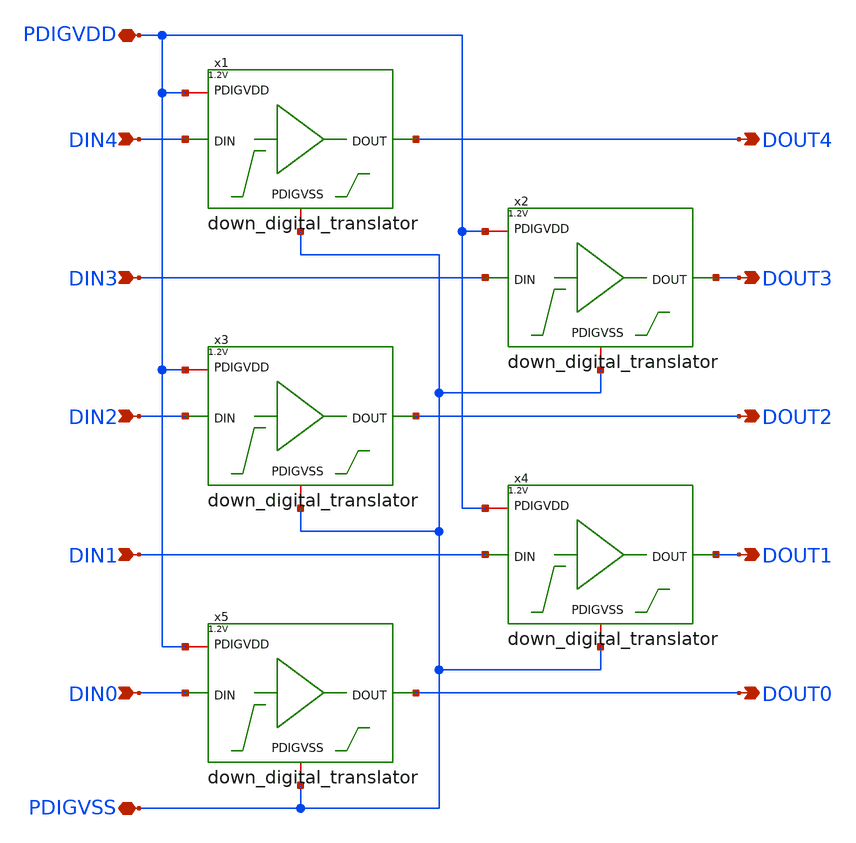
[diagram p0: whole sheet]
** sch_path: xschem/5x_down_digital_translator.sch
**.subckt 5x_down_digital_translator PDIGVDD PDIGVSS DIN3 DIN2 DIN1 DIN0 DIN4 DOUT3 DOUT2 DOUT1
*+ DOUT0 DOUT4
*.iopin PDIGVDD
*.iopin PDIGVSS
*.ipin DIN3
*.ipin DIN2
*.ipin DIN1
*.ipin DIN0
*.ipin DIN4
*.opin DOUT3
*.opin DOUT2
*.opin DOUT1
*.opin DOUT0
*.opin DOUT4
x1 PDIGVDD DIN4 DOUT4 PDIGVSS down_digital_translator
x2 PDIGVDD DIN3 DOUT3 PDIGVSS down_digital_translator
x3 PDIGVDD DIN2 DOUT2 PDIGVSS down_digital_translator
x4 PDIGVDD DIN1 DOUT1 PDIGVSS down_digital_translator
x5 PDIGVDD DIN0 DOUT0 PDIGVSS down_digital_translator
**.ends

* expanding   symbol:  down_digital_translator.sym # of pins=4
** sym_path: xschem/down_digital_translator.sym
** sch_path: xschem/down_digital_translator.sch
.subckt down_digital_translator PDIGVDD DIN DOUT PDIGVSS
*.iopin PDIGVDD
*.ipin DIN
*.opin DOUT
*.iopin PDIGVSS
XM1 net1 DIN PDIGVSS PDIGVSS sg13_hv_nmos w=0.3u l=0.45u ng=1 m=1 mm_ok=1
XM2 net1 DIN PDIGVDD PDIGVDD sg13_hv_pmos w=0.6u l=0.45u ng=1 m=1 mm_ok=1
XM3 DOUT net1 PDIGVSS PDIGVSS sg13_hv_nmos w=0.3u l=0.45u ng=1 m=1 mm_ok=1
XM4 DOUT net1 PDIGVDD PDIGVDD sg13_hv_pmos w=0.6u l=0.45u ng=1 m=1 mm_ok=1
.ends

.end
